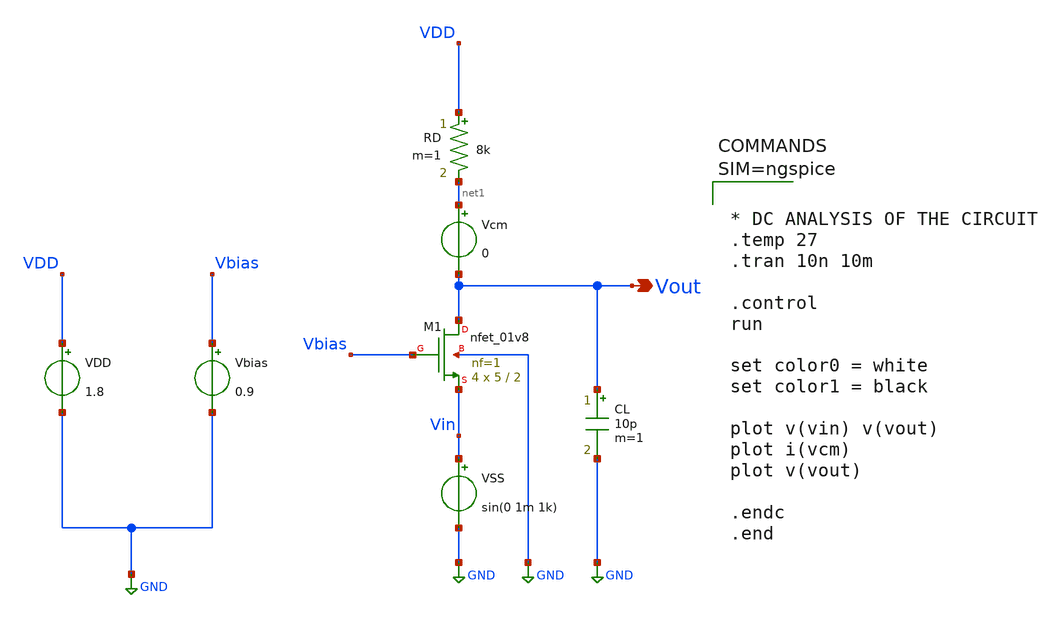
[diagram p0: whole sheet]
** sch_path: Common_Gate_MOS_Amps/Common_Gate_Amp_AC_Transient_Analysis.sch
**.subckt Common_Gate_Amp_AC_Transient_Analysis Vout
*.opin Vout
XM1 Vout Vbias Vin GND sky130_fd_pr__nfet_01v8 L=2 W=5 nf=1 ad='int((1 + 1)/2) * 5 / 1 * 0.29' as='int((1 + 2)/2) * 5 / 1 * 0.29'
+ pd='2*int((1 + 1)/2) * (5 / 1 + 0.29)' ps='2*int((1 + 2)/2) * (5 / 1 + 0.29)' nrd='0.29 / 5 ' nrs='0.29 / 5 '
+ sa=0 sb=0 sd=0 mult=4 m=4
RD VDD net1 8k m=1
CL Vout GND 10p m=1
VDD VDD GND 1.8
Vbias Vbias GND 0.9
VSS Vin GND sin(0 1m 1k)
Vcm net1 Vout 0
**** begin user architecture code

** opencircuitdesign pdks install
.lib $::SKYWATER_MODELS/sky130.lib.spice tt




* DC ANALYSIS OF THE CIRCUIT
.temp 27
.tran 10n 10m

.control
run

set color0 = white
set color1 = black

plot v(vin) v(vout)
plot i(vcm)
plot v(vout)

.endc
.end




**** end user architecture code
**.ends
.GLOBAL GND
.end
